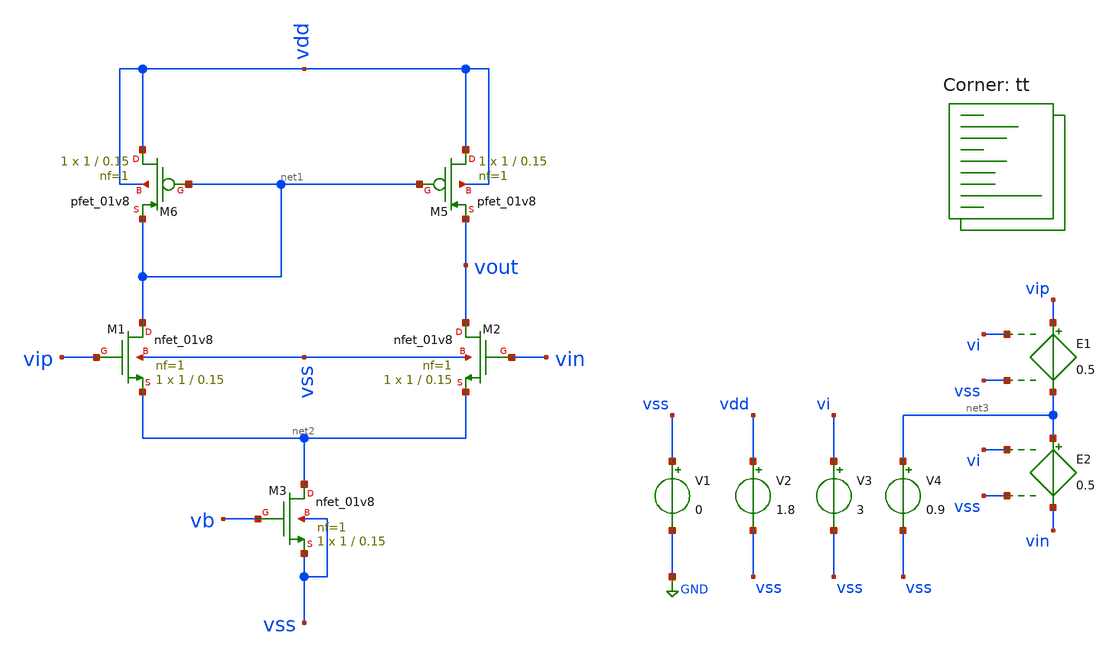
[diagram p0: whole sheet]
** sch_path: sky130/pre_layout_sim/ota_local_test.sch
**.subckt ota_local_test
XM1 net1 vip net2 vss sky130_fd_pr__nfet_01v8 L=0.15 W=1 nf=1 ad='int((1 + 1)/2) * 1 / 1 * 0.29' as='int((1 + 2)/2) * 1 / 1 * 0.29'
+ pd='2*int((1 + 1)/2) * (1 / 1 + 0.29)' ps='2*int((1 + 2)/2) * (1 / 1 + 0.29)' nrd='0.29 / 1 ' nrs='0.29 / 1 '
+ sa=0 sb=0 sd=0 mult=1 m=1
XM2 vout vin net2 vss sky130_fd_pr__nfet_01v8 L=0.15 W=1 nf=1 ad='int((1 + 1)/2) * 1 / 1 * 0.29' as='int((1 + 2)/2) * 1 / 1 * 0.29'
+ pd='2*int((1 + 1)/2) * (1 / 1 + 0.29)' ps='2*int((1 + 2)/2) * (1 / 1 + 0.29)' nrd='0.29 / 1 ' nrs='0.29 / 1 '
+ sa=0 sb=0 sd=0 mult=1 m=1
XM3 net2 vb vss vss sky130_fd_pr__nfet_01v8 L=0.15 W=1 nf=1 ad='int((1 + 1)/2) * 1 / 1 * 0.29' as='int((1 + 2)/2) * 1 / 1 * 0.29'
+ pd='2*int((1 + 1)/2) * (1 / 1 + 0.29)' ps='2*int((1 + 2)/2) * (1 / 1 + 0.29)' nrd='0.29 / 1 ' nrs='0.29 / 1 '
+ sa=0 sb=0 sd=0 mult=1 m=1
XM5 vdd net1 vout vdd sky130_fd_pr__pfet_01v8 L=0.15 W=1 nf=1 ad='int((1 + 1)/2) * 1 / 1 * 0.29' as='int((1 + 2)/2) * 1 / 1 * 0.29'
+ pd='2*int((1 + 1)/2) * (1 / 1 + 0.29)' ps='2*int((1 + 2)/2) * (1 / 1 + 0.29)' nrd='0.29 / 1 ' nrs='0.29 / 1 '
+ sa=0 sb=0 sd=0 mult=1 m=1
XM6 vdd net1 net1 vdd sky130_fd_pr__pfet_01v8 L=0.15 W=1 nf=1 ad='int((1 + 1)/2) * 1 / 1 * 0.29' as='int((1 + 2)/2) * 1 / 1 * 0.29'
+ pd='2*int((1 + 1)/2) * (1 / 1 + 0.29)' ps='2*int((1 + 2)/2) * (1 / 1 + 0.29)' nrd='0.29 / 1 ' nrs='0.29 / 1 '
+ sa=0 sb=0 sd=0 mult=1 m=1
V1 vss GND 0
V2 vdd vss 1.8
V3 vi vss 3
E1 vip net3 vi vss 0.5
V4 net3 vss 0.9
E2 net3 vin vi vss 0.5
**** begin user architecture code

blabla


** opencircuitdesign pdks install
.lib $::SKYWATER_MODELS/sky130.lib.spice tt

.lib $::SKYWATER_MODELS/sky130.lib.spice tt
**** end user architecture code
**.ends
.GLOBAL GND
.end
